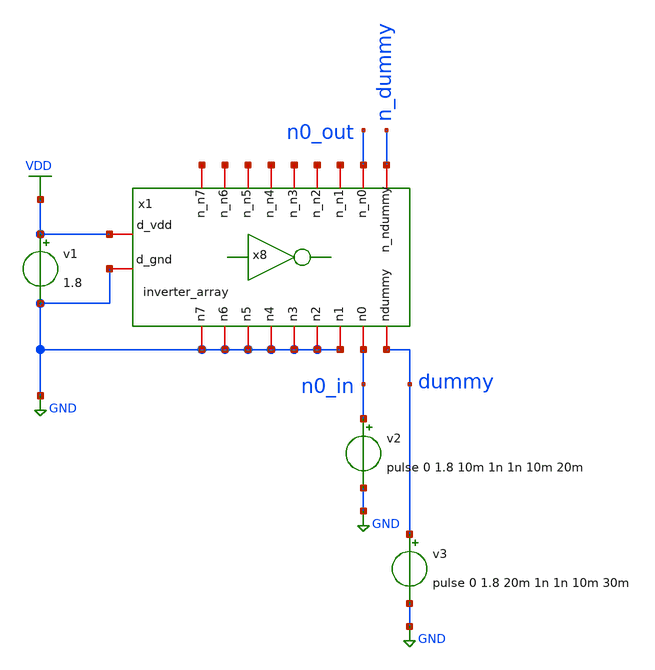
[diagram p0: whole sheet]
** sch_path: Xschem/Schematics/ADC/simulations_elements/deprecated/ADC.sch
**.subckt ADC
v1 VDD GND 1.8
v2 n0_in GND pulse 0 1.8 10m 1n 1n 10m 20m
v3 dummy GND pulse 0 1.8 20m 1n 1n 10m 30m
x1 n0_out net1 net2 net3 net4 net5 net6 net7 n_dummy VDD GND GND GND dummy n0_in GND GND GND GND GND
+ inverter_array
**** begin user architecture code

** opencircuitdesign pdks install
.lib $::SKYWATER_MODELS/sky130.lib.spice tt

**** end user architecture code
**.ends
.GLOBAL GND
.GLOBAL VDD
**** begin user architecture code

* .option SCALE=1e-6
.option method=gear seed=12
.control
save all
tran 0.1m 30m
write ADC.raw
plot n0_in n0_out
.endc


**** end user architecture code
.end
